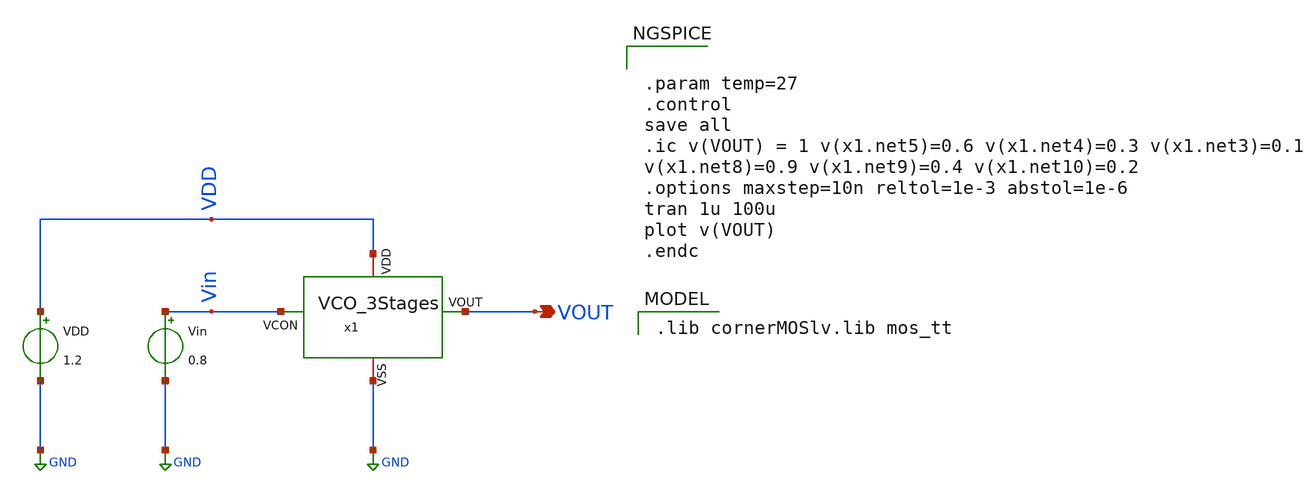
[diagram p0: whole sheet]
** sch_path: Team 1 Design/design_data/xschem/VCO/VCO_3Stages_tb.sch
**.subckt VCO_3Stages_tb VOUT
*.opin VOUT
x1 VDD VOUT Vin GND VCO_3Stages
VDD VDD GND 1.2
Vin Vin GND 0.8
**** begin user architecture code


.param temp=27
.control
save all
.ic v(VOUT) = 1 v(x1.net5)=0.6 v(x1.net4)=0.3 v(x1.net3)=0.1
v(x1.net8)=0.9 v(x1.net9)=0.4 v(x1.net10)=0.2
.options maxstep=10n reltol=1e-3 abstol=1e-6
tran 1u 100u
plot v(VOUT)
.endc


 .lib cornerMOSlv.lib mos_tt

**** end user architecture code
**.ends
.GLOBAL GND
.end
